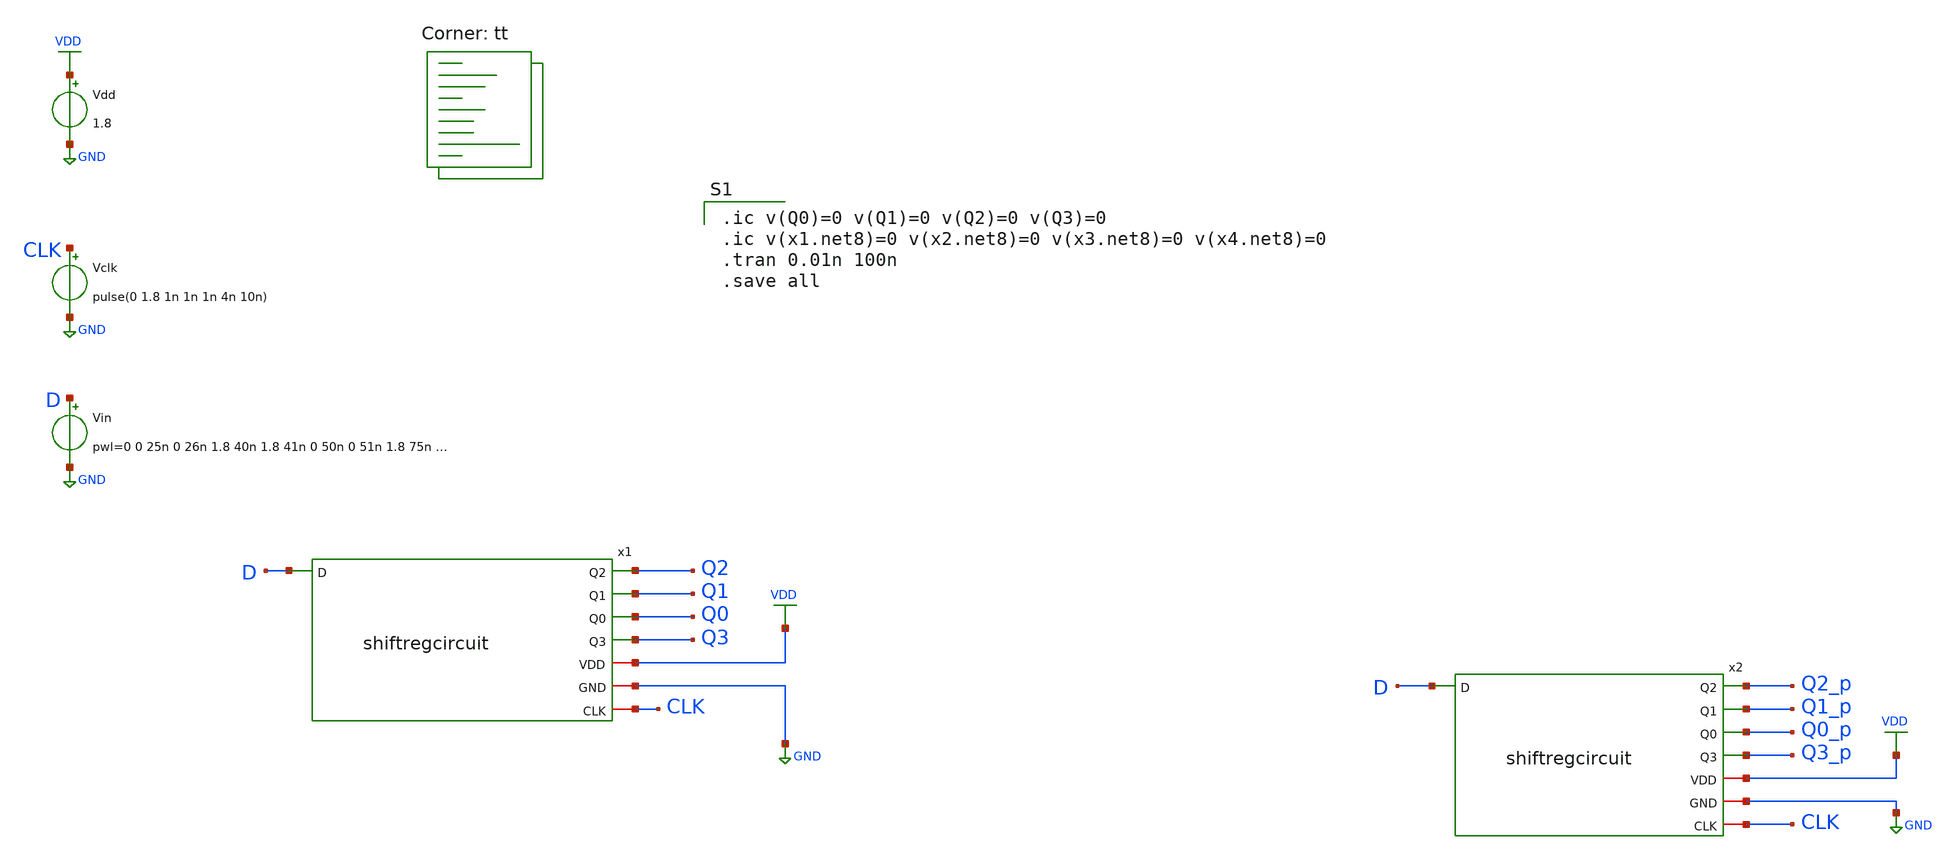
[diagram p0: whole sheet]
** sch_path: shiftreg_tb.sch
**.subckt shiftreg_tb
Vdd VDD GND 1.8
Vclk CLK GND pulse(0 1.8 1n 1n 1n 4n 10n)
Vin D GND pwl=0 0 25n 0 26n 1.8 40n 1.8 41n 0 50n 0 51n 1.8 75n 1.8 76n 0
x1 Q2 Q1 Q0 Q3 VDD D GND CLK shiftregcircuit
x2 Q2_p Q1_p Q0_p Q3_p VDD D GND CLK shiftregcircuit
**** begin user architecture code
.lib $::SKYWATER_MODELS/sky130.lib.spice tt

.ic v(Q0)=0 v(Q1)=0 v(Q2)=0 v(Q3)=0
.ic v(x1.net8)=0 v(x2.net8)=0 v(x3.net8)=0 v(x4.net8)=0
.tran 0.01n 100n
.save all

**** end user architecture code
**.ends

* expanding   symbol:  shiftregcircuit.sym # of pins=8
** sym_path: shiftregcircuit.sym
** sch_path: shiftregcircuit.sch
.subckt shiftregcircuit Q2 Q1 Q0 Q3 VDD D GND CLK
*.ipin D
*.opin Q0
*.opin Q1
*.opin Q2
*.opin Q3
*.iopin VDD
*.iopin GND
*.iopin CLK
x1 VDD Dn Qn0 D Q0 Dn GND CLK d-flipflop
x2 VDD Qn0 Qn1 Q0 Q1 Qn0 GND CLK d-flipflop
x3 VDD Qn1 Qn2 Q1 Q2 Qn1 GND CLK d-flipflop
x4 VDD Qn2 Qn3 Q2 Q3 Qn2 GND CLK d-flipflop
X5 net1 net2 inv_vtc
.ends


* expanding   symbol:  d-flipflop.sym # of pins=8
** sym_path: d-flipflop.sym
** sch_path: d-flipflop.sch
.subckt d-flipflop VP Dn1 Qb1 D Q Dn2 VN CLK
*.ipin D
*.ipin Dn1
*.opin Qb1
*.opin Q
*.ipin CLK
*.ipin Dn2
*.iopin VP
*.iopin VN
XM1 VN Dn2 net7 VN sky130_fd_pr__nfet_01v8 L=0.15 W=1 nf=1 ad='int((nf+1)/2) * W/nf * 0.29' as='int((nf+2)/2) * W/nf * 0.29'
+ pd='2*int((nf+1)/2) * (W/nf + 0.29)' ps='2*int((nf+2)/2) * (W/nf + 0.29)' nrd='0.29 / W' nrs='0.29 / W'
+ sa=0 sb=0 sd=0 mult=1 m=1
XM2 net7 CLK net8 VN sky130_fd_pr__nfet_01v8 L=0.15 W=1 nf=1 ad='int((nf+1)/2) * W/nf * 0.29' as='int((nf+2)/2) * W/nf * 0.29'
+ pd='2*int((nf+1)/2) * (W/nf + 0.29)' ps='2*int((nf+2)/2) * (W/nf + 0.29)' nrd='0.29 / W' nrs='0.29 / W'
+ sa=0 sb=0 sd=0 mult=1 m=1
XM3 VN net4 net8 VN sky130_fd_pr__nfet_01v8 L=0.15 W=1 nf=1 ad='int((nf+1)/2) * W/nf * 0.29' as='int((nf+2)/2) * W/nf * 0.29'
+ pd='2*int((nf+1)/2) * (W/nf + 0.29)' ps='2*int((nf+2)/2) * (W/nf + 0.29)' nrd='0.29 / W' nrs='0.29 / W'
+ sa=0 sb=0 sd=0 mult=1 m=1
XM4 net3 D VN VN sky130_fd_pr__nfet_01v8 L=0.15 W=1 nf=1 ad='int((nf+1)/2) * W/nf * 0.29' as='int((nf+2)/2) * W/nf * 0.29'
+ pd='2*int((nf+1)/2) * (W/nf + 0.29)' ps='2*int((nf+2)/2) * (W/nf + 0.29)' nrd='0.29 / W' nrs='0.29 / W'
+ sa=0 sb=0 sd=0 mult=1 m=1
XM5 net3 CLK net4 VN sky130_fd_pr__nfet_01v8 L=0.15 W=1 nf=1 ad='int((nf+1)/2) * W/nf * 0.29' as='int((nf+2)/2) * W/nf * 0.29'
+ pd='2*int((nf+1)/2) * (W/nf + 0.29)' ps='2*int((nf+2)/2) * (W/nf + 0.29)' nrd='0.29 / W' nrs='0.29 / W'
+ sa=0 sb=0 sd=0 mult=1 m=1
XM6 VN net8 net4 VN sky130_fd_pr__nfet_01v8 L=0.15 W=1 nf=1 ad='int((nf+1)/2) * W/nf * 0.29' as='int((nf+2)/2) * W/nf * 0.29'
+ pd='2*int((nf+1)/2) * (W/nf + 0.29)' ps='2*int((nf+2)/2) * (W/nf + 0.29)' nrd='0.29 / W' nrs='0.29 / W'
+ sa=0 sb=0 sd=0 mult=1 m=1
XM7 net9 net8 VN VN sky130_fd_pr__nfet_01v8 L=0.15 W=1 nf=1 ad='int((nf+1)/2) * W/nf * 0.29' as='int((nf+2)/2) * W/nf * 0.29'
+ pd='2*int((nf+1)/2) * (W/nf + 0.29)' ps='2*int((nf+2)/2) * (W/nf + 0.29)' nrd='0.29 / W' nrs='0.29 / W'
+ sa=0 sb=0 sd=0 mult=1 m=1
XM8 VN CLK net9 VN sky130_fd_pr__nfet_01v8 L=0.15 W=1 nf=1 ad='int((nf+1)/2) * W/nf * 0.29' as='int((nf+2)/2) * W/nf * 0.29'
+ pd='2*int((nf+1)/2) * (W/nf + 0.29)' ps='2*int((nf+2)/2) * (W/nf + 0.29)' nrd='0.29 / W' nrs='0.29 / W'
+ sa=0 sb=0 sd=0 mult=1 m=1
XM9 Qb1 Q net9 VN sky130_fd_pr__nfet_01v8 L=0.15 W=1 nf=1 ad='int((nf+1)/2) * W/nf * 0.29' as='int((nf+2)/2) * W/nf * 0.29'
+ pd='2*int((nf+1)/2) * (W/nf + 0.29)' ps='2*int((nf+2)/2) * (W/nf + 0.29)' nrd='0.29 / W' nrs='0.29 / W'
+ sa=0 sb=0 sd=0 mult=1 m=1
XM10 VN net4 net5 VN sky130_fd_pr__nfet_01v8 L=0.15 W=1 nf=1 ad='int((nf+1)/2) * W/nf * 0.29' as='int((nf+2)/2) * W/nf * 0.29'
+ pd='2*int((nf+1)/2) * (W/nf + 0.29)' ps='2*int((nf+2)/2) * (W/nf + 0.29)' nrd='0.29 / W' nrs='0.29 / W'
+ sa=0 sb=0 sd=0 mult=1 m=1
XM11 VN CLK net5 VN sky130_fd_pr__nfet_01v8 L=0.15 W=1 nf=1 ad='int((nf+1)/2) * W/nf * 0.29' as='int((nf+2)/2) * W/nf * 0.29'
+ pd='2*int((nf+1)/2) * (W/nf + 0.29)' ps='2*int((nf+2)/2) * (W/nf + 0.29)' nrd='0.29 / W' nrs='0.29 / W'
+ sa=0 sb=0 sd=0 mult=1 m=1
XM12 Q Qb1 net5 VN sky130_fd_pr__nfet_01v8 L=0.15 W=1 nf=1 ad='int((nf+1)/2) * W/nf * 0.29' as='int((nf+2)/2) * W/nf * 0.29'
+ pd='2*int((nf+1)/2) * (W/nf + 0.29)' ps='2*int((nf+2)/2) * (W/nf + 0.29)' nrd='0.29 / W' nrs='0.29 / W'
+ sa=0 sb=0 sd=0 mult=1 m=1
XM13 VP D net2 VP sky130_fd_pr__pfet_01v8 L=0.15 W=1 nf=1 ad='int((nf+1)/2) * W/nf * 0.29' as='int((nf+2)/2) * W/nf * 0.29'
+ pd='2*int((nf+1)/2) * (W/nf + 0.29)' ps='2*int((nf+2)/2) * (W/nf + 0.29)' nrd='0.29 / W' nrs='0.29 / W'
+ sa=0 sb=0 sd=0 mult=1 m=1
XM14 net2 CLK VP VP sky130_fd_pr__pfet_01v8 L=0.15 W=1 nf=1 ad='int((nf+1)/2) * W/nf * 0.29' as='int((nf+2)/2) * W/nf * 0.29'
+ pd='2*int((nf+1)/2) * (W/nf + 0.29)' ps='2*int((nf+2)/2) * (W/nf + 0.29)' nrd='0.29 / W' nrs='0.29 / W'
+ sa=0 sb=0 sd=0 mult=1 m=1
XM15 net4 net8 net2 VP sky130_fd_pr__pfet_01v8 L=0.15 W=1 nf=1 ad='int((nf+1)/2) * W/nf * 0.29' as='int((nf+2)/2) * W/nf * 0.29'
+ pd='2*int((nf+1)/2) * (W/nf + 0.29)' ps='2*int((nf+2)/2) * (W/nf + 0.29)' nrd='0.29 / W' nrs='0.29 / W'
+ sa=0 sb=0 sd=0 mult=1 m=1
XM16 net1 Dn1 VP VP sky130_fd_pr__pfet_01v8 L=0.15 W=1 nf=1 ad='int((nf+1)/2) * W/nf * 0.29' as='int((nf+2)/2) * W/nf * 0.29'
+ pd='2*int((nf+1)/2) * (W/nf + 0.29)' ps='2*int((nf+2)/2) * (W/nf + 0.29)' nrd='0.29 / W' nrs='0.29 / W'
+ sa=0 sb=0 sd=0 mult=1 m=1
XM17 net1 CLK VP VP sky130_fd_pr__pfet_01v8 L=0.15 W=1 nf=1 ad='int((nf+1)/2) * W/nf * 0.29' as='int((nf+2)/2) * W/nf * 0.29'
+ pd='2*int((nf+1)/2) * (W/nf + 0.29)' ps='2*int((nf+2)/2) * (W/nf + 0.29)' nrd='0.29 / W' nrs='0.29 / W'
+ sa=0 sb=0 sd=0 mult=1 m=1
XM18 net8 net4 net1 VP sky130_fd_pr__pfet_01v8 L=0.15 W=1 nf=1 ad='int((nf+1)/2) * W/nf * 0.29' as='int((nf+2)/2) * W/nf * 0.29'
+ pd='2*int((nf+1)/2) * (W/nf + 0.29)' ps='2*int((nf+2)/2) * (W/nf + 0.29)' nrd='0.29 / W' nrs='0.29 / W'
+ sa=0 sb=0 sd=0 mult=1 m=1
XM19 net6 net4 VP VP sky130_fd_pr__pfet_01v8 L=0.15 W=1 nf=1 ad='int((nf+1)/2) * W/nf * 0.29' as='int((nf+2)/2) * W/nf * 0.29'
+ pd='2*int((nf+1)/2) * (W/nf + 0.29)' ps='2*int((nf+2)/2) * (W/nf + 0.29)' nrd='0.29 / W' nrs='0.29 / W'
+ sa=0 sb=0 sd=0 mult=1 m=1
XM20 Q CLK net6 VP sky130_fd_pr__pfet_01v8 L=0.15 W=1 nf=1 ad='int((nf+1)/2) * W/nf * 0.29' as='int((nf+2)/2) * W/nf * 0.29'
+ pd='2*int((nf+1)/2) * (W/nf + 0.29)' ps='2*int((nf+2)/2) * (W/nf + 0.29)' nrd='0.29 / W' nrs='0.29 / W'
+ sa=0 sb=0 sd=0 mult=1 m=1
XM21 VP Qb1 Q VP sky130_fd_pr__pfet_01v8 L=0.15 W=1 nf=1 ad='int((nf+1)/2) * W/nf * 0.29' as='int((nf+2)/2) * W/nf * 0.29'
+ pd='2*int((nf+1)/2) * (W/nf + 0.29)' ps='2*int((nf+2)/2) * (W/nf + 0.29)' nrd='0.29 / W' nrs='0.29 / W'
+ sa=0 sb=0 sd=0 mult=1 m=1
XM22 VP net8 net10 VP sky130_fd_pr__pfet_01v8 L=0.15 W=1 nf=1 ad='int((nf+1)/2) * W/nf * 0.29' as='int((nf+2)/2) * W/nf * 0.29'
+ pd='2*int((nf+1)/2) * (W/nf + 0.29)' ps='2*int((nf+2)/2) * (W/nf + 0.29)' nrd='0.29 / W' nrs='0.29 / W'
+ sa=0 sb=0 sd=0 mult=1 m=1
XM23 Qb1 CLK net10 VP sky130_fd_pr__pfet_01v8 L=0.15 W=1 nf=1 ad='int((nf+1)/2) * W/nf * 0.29' as='int((nf+2)/2) * W/nf * 0.29'
+ pd='2*int((nf+1)/2) * (W/nf + 0.29)' ps='2*int((nf+2)/2) * (W/nf + 0.29)' nrd='0.29 / W' nrs='0.29 / W'
+ sa=0 sb=0 sd=0 mult=1 m=1
XM24 VP Q Qb1 VP sky130_fd_pr__pfet_01v8 L=0.15 W=1 nf=1 ad='int((nf+1)/2) * W/nf * 0.29' as='int((nf+2)/2) * W/nf * 0.29'
+ pd='2*int((nf+1)/2) * (W/nf + 0.29)' ps='2*int((nf+2)/2) * (W/nf + 0.29)' nrd='0.29 / W' nrs='0.29 / W'
+ sa=0 sb=0 sd=0 mult=1 m=1
.ends


* expanding   symbol:  inv_vtc.sym # of pins=2
** sym_path: inv_vtc.sym
** sch_path: inv_vtc.sch
.subckt inv_vtc A Y
*.ipin A
*.opin Y
XM1 Y A VDD VDD sky130_fd_pr__pfet_01v8 L=0.15 W=2 nf=1 ad='int((nf+1)/2) * W/nf * 0.29' as='int((nf+2)/2) * W/nf * 0.29'
+ pd='2*int((nf+1)/2) * (W/nf + 0.29)' ps='2*int((nf+2)/2) * (W/nf + 0.29)' nrd='0.29 / W' nrs='0.29 / W'
+ sa=0 sb=0 sd=0 mult=1 m=1
XM2 Y A GND GND sky130_fd_pr__nfet_01v8 L=0.15 W=1 nf=1 ad='int((nf+1)/2) * W/nf * 0.29' as='int((nf+2)/2) * W/nf * 0.29'
+ pd='2*int((nf+1)/2) * (W/nf + 0.29)' ps='2*int((nf+2)/2) * (W/nf + 0.29)' nrd='0.29 / W' nrs='0.29 / W'
+ sa=0 sb=0 sd=0 mult=1 m=1
.ends

.GLOBAL VDD
.GLOBAL GND
.end
